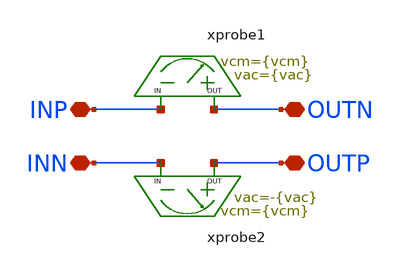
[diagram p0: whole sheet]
** sch_path: schema/ac_diff_probe/ac_diff_probe.sch
**.subckt ac_diff_probe OUTN INP OUTP INN
*.iopin OUTN
*.iopin INP
*.iopin OUTP
*.iopin INN
xprobe1 OUTN INP ac_probe vcm={vcm} vac={vac}
xprobe2 OUTP INN ac_probe vcm={vcm} vac=-{vac}
**.ends

* expanding   symbol:  /foss/designs/Chipalooza2/schema/ac_probe/ac_probe.sym # of pins=2
** sym_path: schema/ac_probe/ac_probe.sym
** sch_path: schema/ac_probe/ac_probe.sch
.subckt ac_probe OUT IN  vcm=0.75 vac=0.01

*.iopin IN
*.iopin OUT
C1 net1 IN 1 m=1
V1 net1 0 {vcm} ac {vac}
L1 OUT net2 1G m=1
R1 net2 IN 1m m=1
.ends

.end
